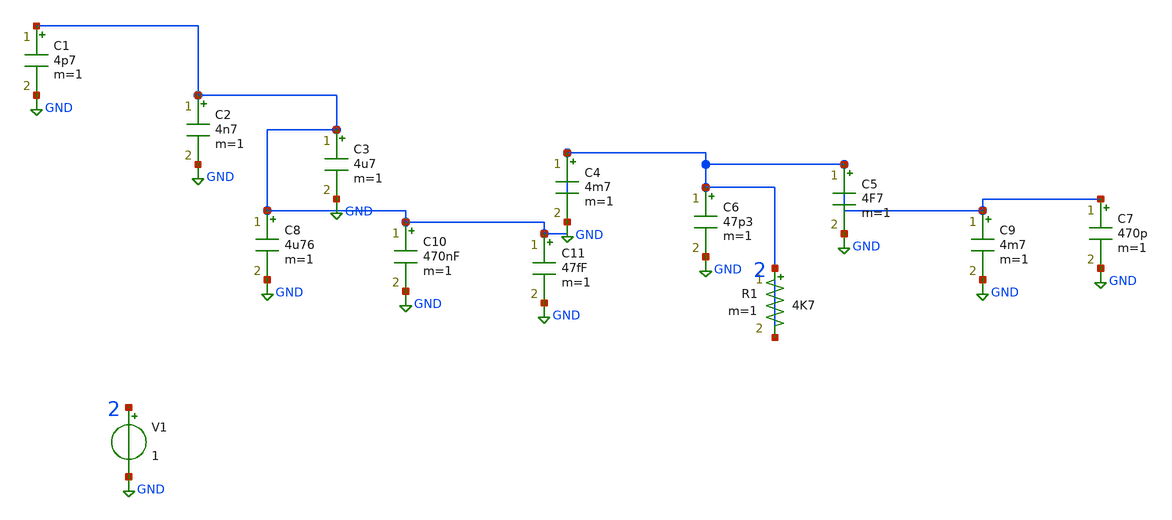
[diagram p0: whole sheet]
** sch_path: data/sch/aicas_RKM-C-1.sch
**.subckt aicas_RKM-C-1
V1 2 GND 1
R1 2 2 4K7 m=1
C1 2 GND 4p7 m=1
C2 2 GND 4n7 m=1
C3 2 GND 4u7 m=1
C4 2 2 4m7 m=1
C5 2 GND 4F7 m=1
C6 2 GND 47p3 m=1
C7 2 GND 470p m=1
C8 2 GND 4u76 m=1
C9 2 GND 4m7 m=1
C10 2 GND 470nF m=1
C11 2 GND 47fF m=1
**.ends
.GLOBAL GND
.end
